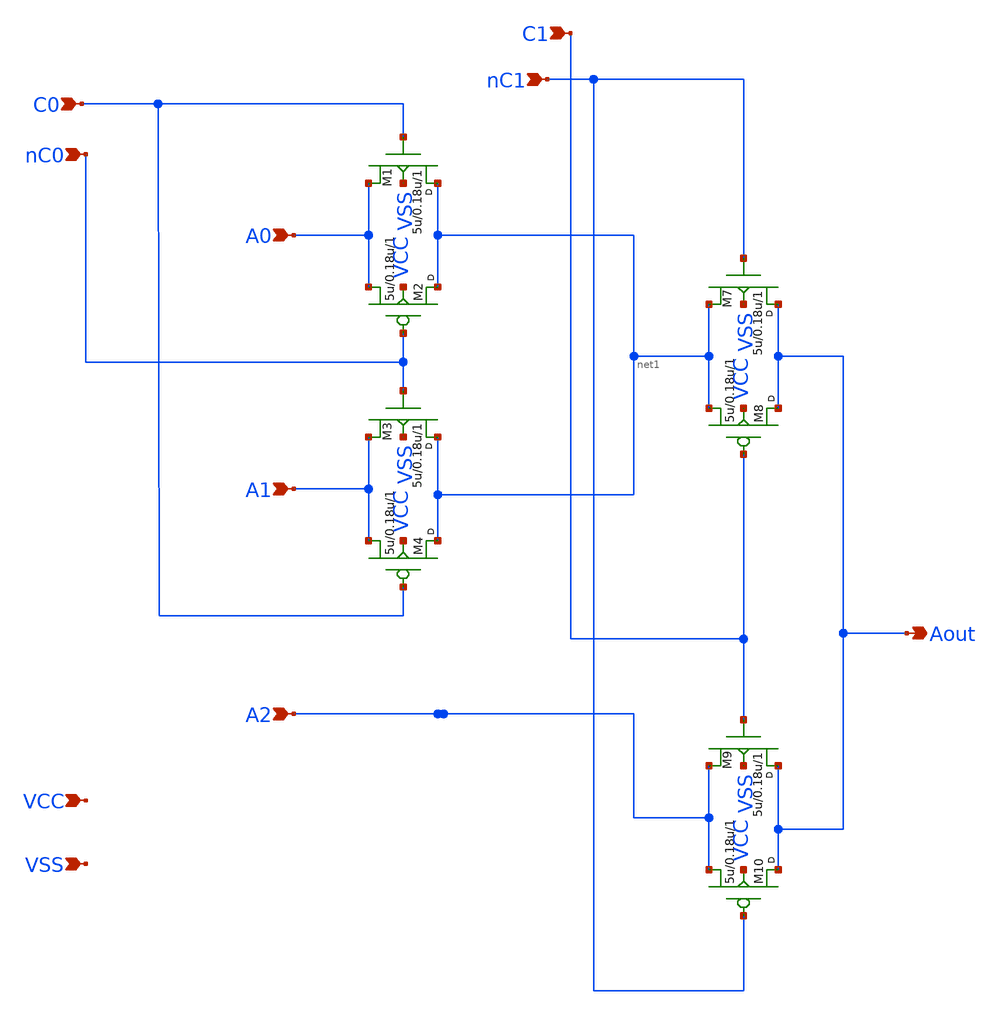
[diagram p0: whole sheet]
** sch_path: Analog_Mux.sch
**.subckt Analog_Mux C0 C1 A0 A2 A1 nC0 nC1 Aout VCC VSS
*.ipin C0
*.ipin C1
*.ipin A0
*.ipin A2
*.ipin A1
*.ipin nC0
*.ipin nC1
*.opin Aout
*.ipin VCC
*.ipin VSS
M1 net1 C0 A0 VSS nmos w=5u l=0.18u m=1
M2 net1 nC0 A0 VCC pmos w=5u l=0.18u m=1
M3 net1 nC0 A1 VSS nmos w=5u l=0.18u m=1
M4 net1 C0 A1 VCC pmos w=5u l=0.18u m=1
M7 Aout nC1 net1 VSS nmos w=5u l=0.18u m=1
M8 Aout C1 net1 VCC pmos w=5u l=0.18u m=1
M9 Aout C1 A2 VSS nmos w=5u l=0.18u m=1
M10 Aout nC1 A2 VCC pmos w=5u l=0.18u m=1
**.ends
.end
